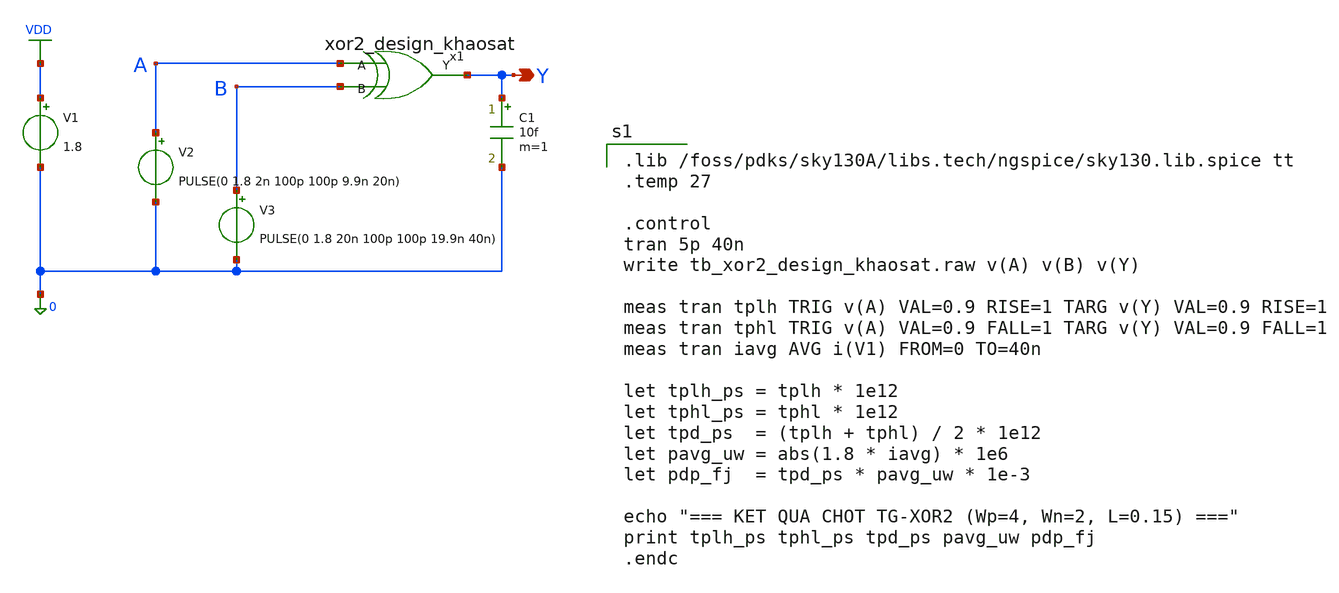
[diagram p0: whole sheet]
** sch_path: cells/full_adder_tg/xschem/tb_xor2_design_khaosat.sch
**.subckt tb_xor2_design_khaosat Y
*.opin Y
V1 VDD 0 1.8
V2 A 0 PULSE(0 1.8 2n 100p 100p 9.9n 20n)
V3 B 0 PULSE(0 1.8 20n 100p 100p 19.9n 40n)
x1 B A Y xor2_design_khaosat
C1 Y 0 10f m=1
**.ends

* expanding   symbol:  ./xor2_design_khaosat.sym # of pins=3
** sym_path: cells/full_adder_tg/xschem/xor2_design_khaosat.sym
** sch_path: cells/full_adder_tg/xschem/xor2_design_khaosat.sch
.subckt xor2_design_khaosat B A Y
*.opin Y
*.ipin B
*.ipin A
XMPmos_inv_1 net1 B VDD VDD sky130_fd_pr__pfet_01v8 L=0.15 W=5 nf=1 ad='int((1 + 1)/2) * 5 / 1 * 0.29'
+ as='int((1 + 2)/2) * 5 / 1 * 0.29' pd='2*int((1 + 1)/2) * (5 / 1 + 0.29)' ps='2*int((1 + 2)/2) * (5 / 1 + 0.29)'
+ nrd='0.29 / 5 ' nrs='0.29 / 5 ' sa=0 sb=0 sd=0 mult=1 m=1
XMNmos_inv_1 net1 B 0 0 sky130_fd_pr__nfet_01v8 L=0.15 W=2 nf=1 ad='int((1 + 1)/2) * 2 / 1 * 0.29' as='int((1 + 2)/2) * 2 / 1 * 0.29'
+ pd='2*int((1 + 1)/2) * (2 / 1 + 0.29)' ps='2*int((1 + 2)/2) * (2 / 1 + 0.29)' nrd='0.29 / 2 ' nrs='0.29 / 2 '
+ sa=0 sb=0 sd=0 mult=1 m=1
XMPmos_xor_1 Y B A VDD sky130_fd_pr__pfet_01v8 L=0.15 W=5 nf=1 ad='int((1 + 1)/2) * 5 / 1 * 0.29' as='int((1 + 2)/2) * 5 / 1 * 0.29'
+ pd='2*int((1 + 1)/2) * (5 / 1 + 0.29)' ps='2*int((1 + 2)/2) * (5 / 1 + 0.29)' nrd='0.29 / 5 ' nrs='0.29 / 5 '
+ sa=0 sb=0 sd=0 mult=1 m=1
XMNmos_xor_1 Y net1 A 0 sky130_fd_pr__nfet_01v8 L=0.15 W=2 nf=1 ad='int((1 + 1)/2) * 2 / 1 * 0.29' as='int((1 + 2)/2) * 2 / 1 * 0.29'
+ pd='2*int((1 + 1)/2) * (2 / 1 + 0.29)' ps='2*int((1 + 2)/2) * (2 / 1 + 0.29)' nrd='0.29 / 2 ' nrs='0.29 / 2 '
+ sa=0 sb=0 sd=0 mult=1 m=1
XMPmos_xor_2 Y A B VDD sky130_fd_pr__pfet_01v8 L=0.15 W=5 nf=1 ad='int((1 + 1)/2) * 5 / 1 * 0.29' as='int((1 + 2)/2) * 5 / 1 * 0.29'
+ pd='2*int((1 + 1)/2) * (5 / 1 + 0.29)' ps='2*int((1 + 2)/2) * (5 / 1 + 0.29)' nrd='0.29 / 5 ' nrs='0.29 / 5 '
+ sa=0 sb=0 sd=0 mult=1 m=1
XMNmos_xor_2 Y A net1 0 sky130_fd_pr__nfet_01v8 L=0.15 W=2 nf=1 ad='int((1 + 1)/2) * 2 / 1 * 0.29' as='int((1 + 2)/2) * 2 / 1 * 0.29'
+ pd='2*int((1 + 1)/2) * (2 / 1 + 0.29)' ps='2*int((1 + 2)/2) * (2 / 1 + 0.29)' nrd='0.29 / 2 ' nrs='0.29 / 2 '
+ sa=0 sb=0 sd=0 mult=1 m=1
.ends

.GLOBAL VDD
**** begin user architecture code

.lib /foss/pdks/sky130A/libs.tech/ngspice/sky130.lib.spice tt
.temp 27

.control
tran 5p 40n
write tb_xor2_design_khaosat.raw v(A) v(B) v(Y)

meas tran tplh TRIG v(A) VAL=0.9 RISE=1 TARG v(Y) VAL=0.9 RISE=1
meas tran tphl TRIG v(A) VAL=0.9 FALL=1 TARG v(Y) VAL=0.9 FALL=1
meas tran iavg AVG i(V1) FROM=0 TO=40n

let tplh_ps = tplh * 1e12
let tphl_ps = tphl * 1e12
let tpd_ps  = (tplh + tphl) / 2 * 1e12
let pavg_uw = abs(1.8 * iavg) * 1e6
let pdp_fj  = tpd_ps * pavg_uw * 1e-3

echo "=== KET QUA CHOT TG-XOR2 (Wp=4, Wn=2, L=0.15) ==="
print tplh_ps tphl_ps tpd_ps pavg_uw pdp_fj
.endc

**** end user architecture code
.end
